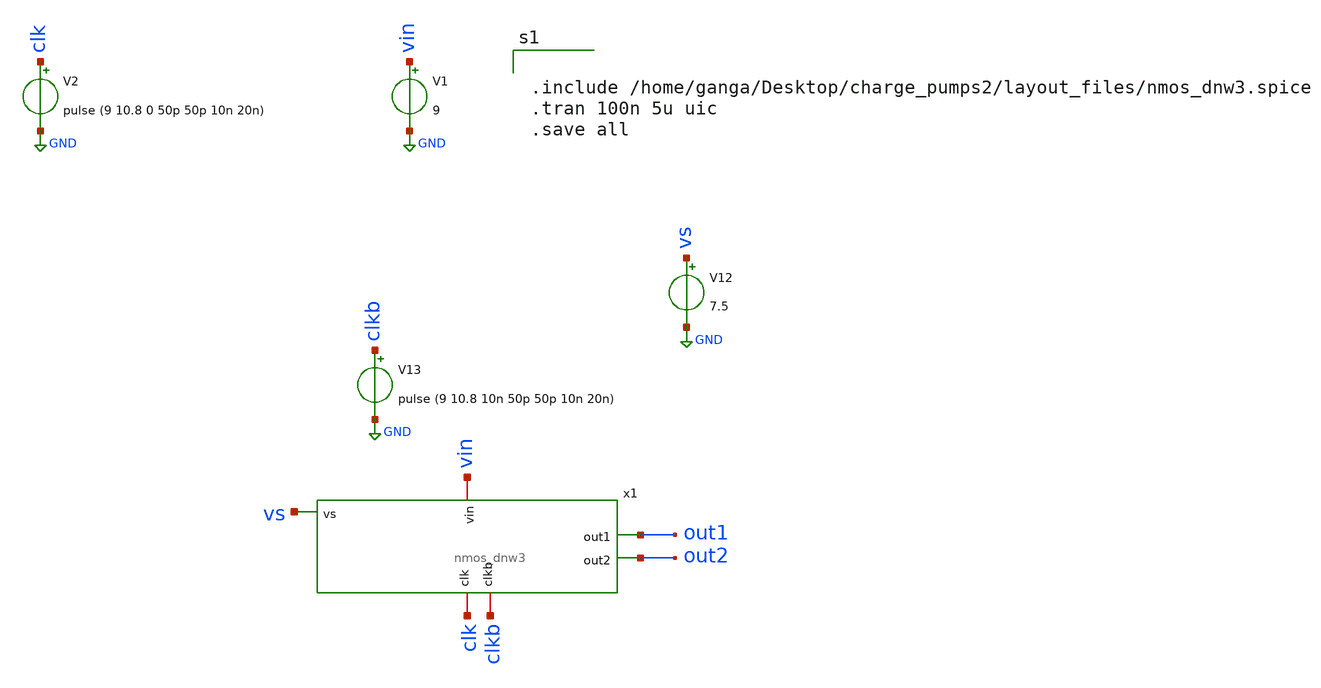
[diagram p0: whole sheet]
** sch_path: xschem/nmos_dnw_tb.sch
**.subckt nmos_dnw_tb
x1 vin out1 out2 clk clkb vs nmos_dnw3
V1 vin GND 9
V2 clk GND pulse (9 10.8 0 50p 50p 10n 20n)
V12 vs GND 7.5
V13 clkb GND pulse (9 10.8 10n 50p 50p 10n 20n)
**** begin user architecture code

** opencircuitdesign pdks install
.lib $::SKYWATER_MODELS/sky130.lib.spice tt




.include /home/ganga/Desktop/charge_pumps2/layout_files/nmos_dnw3.spice
.tran 100n 5u uic
.save all


**** end user architecture code
**.ends
.GLOBAL GND
.end
